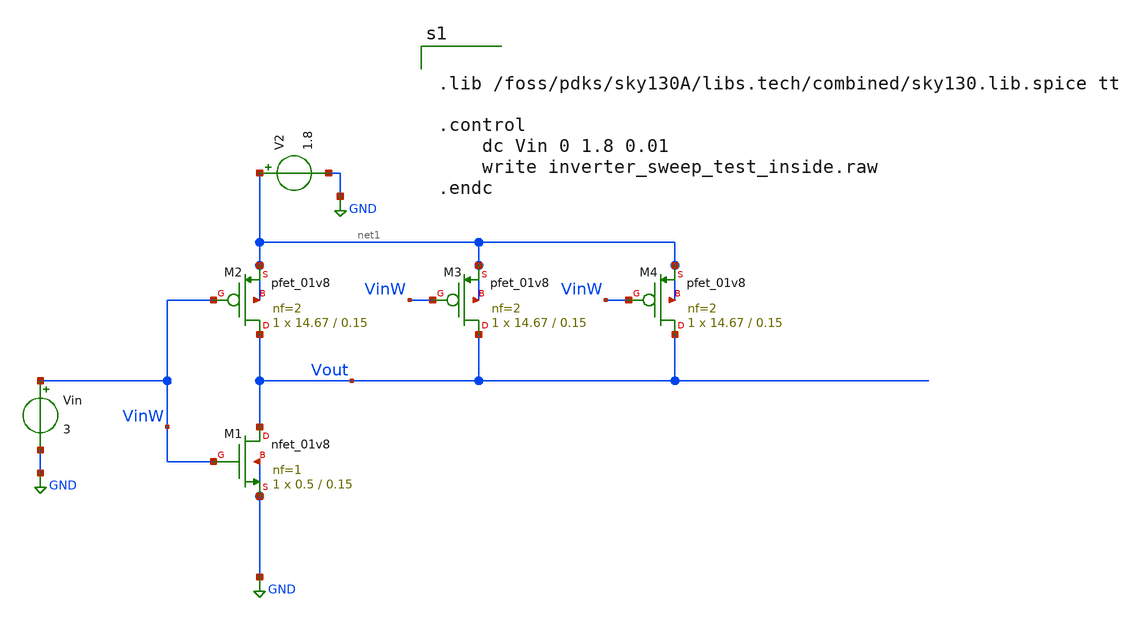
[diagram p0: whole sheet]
** sch_path: xschem/unit_inverter_test_inside.sch
**.subckt unit_inverter_test_inside
XM1 Vout VinW GND GND sky130_fd_pr__nfet_01v8 L=0.15 W=0.5 nf=1 ad='int((nf+1)/2) * W/nf * 0.29' as='int((nf+2)/2) * W/nf * 0.29'
+ pd='2*int((nf+1)/2) * (W/nf + 0.29)' ps='2*int((nf+2)/2) * (W/nf + 0.29)' nrd='0.29 / W' nrs='0.29 / W'
+ sa=0 sb=0 sd=0 mult=1 m=1
XM2 Vout VinW net1 net1 sky130_fd_pr__pfet_01v8 L=0.15 W=14.67 nf=2 ad='int((nf+1)/2) * W/nf * 0.29'
+ as='int((nf+2)/2) * W/nf * 0.29' pd='2*int((nf+1)/2) * (W/nf + 0.29)' ps='2*int((nf+2)/2) * (W/nf + 0.29)'
+ nrd='0.29 / W' nrs='0.29 / W' sa=0 sb=0 sd=0 mult=1 m=1
Vin VinW GND 3
V2 net1 GND 1.8
XM3 Vout VinW net1 net1 sky130_fd_pr__pfet_01v8 L=0.15 W=14.67 nf=2 ad='int((nf+1)/2) * W/nf * 0.29'
+ as='int((nf+2)/2) * W/nf * 0.29' pd='2*int((nf+1)/2) * (W/nf + 0.29)' ps='2*int((nf+2)/2) * (W/nf + 0.29)'
+ nrd='0.29 / W' nrs='0.29 / W' sa=0 sb=0 sd=0 mult=1 m=1
XM4 Vout VinW net1 net1 sky130_fd_pr__pfet_01v8 L=0.15 W=14.67 nf=2 ad='int((nf+1)/2) * W/nf * 0.29'
+ as='int((nf+2)/2) * W/nf * 0.29' pd='2*int((nf+1)/2) * (W/nf + 0.29)' ps='2*int((nf+2)/2) * (W/nf + 0.29)'
+ nrd='0.29 / W' nrs='0.29 / W' sa=0 sb=0 sd=0 mult=1 m=1
**** begin user architecture code


.lib /foss/pdks/sky130A/libs.tech/combined/sky130.lib.spice tt

.control
	dc Vin 0 1.8 0.01
	write inverter_sweep_test_inside.raw
.endc


**** end user architecture code
**.ends
.GLOBAL GND
.end
